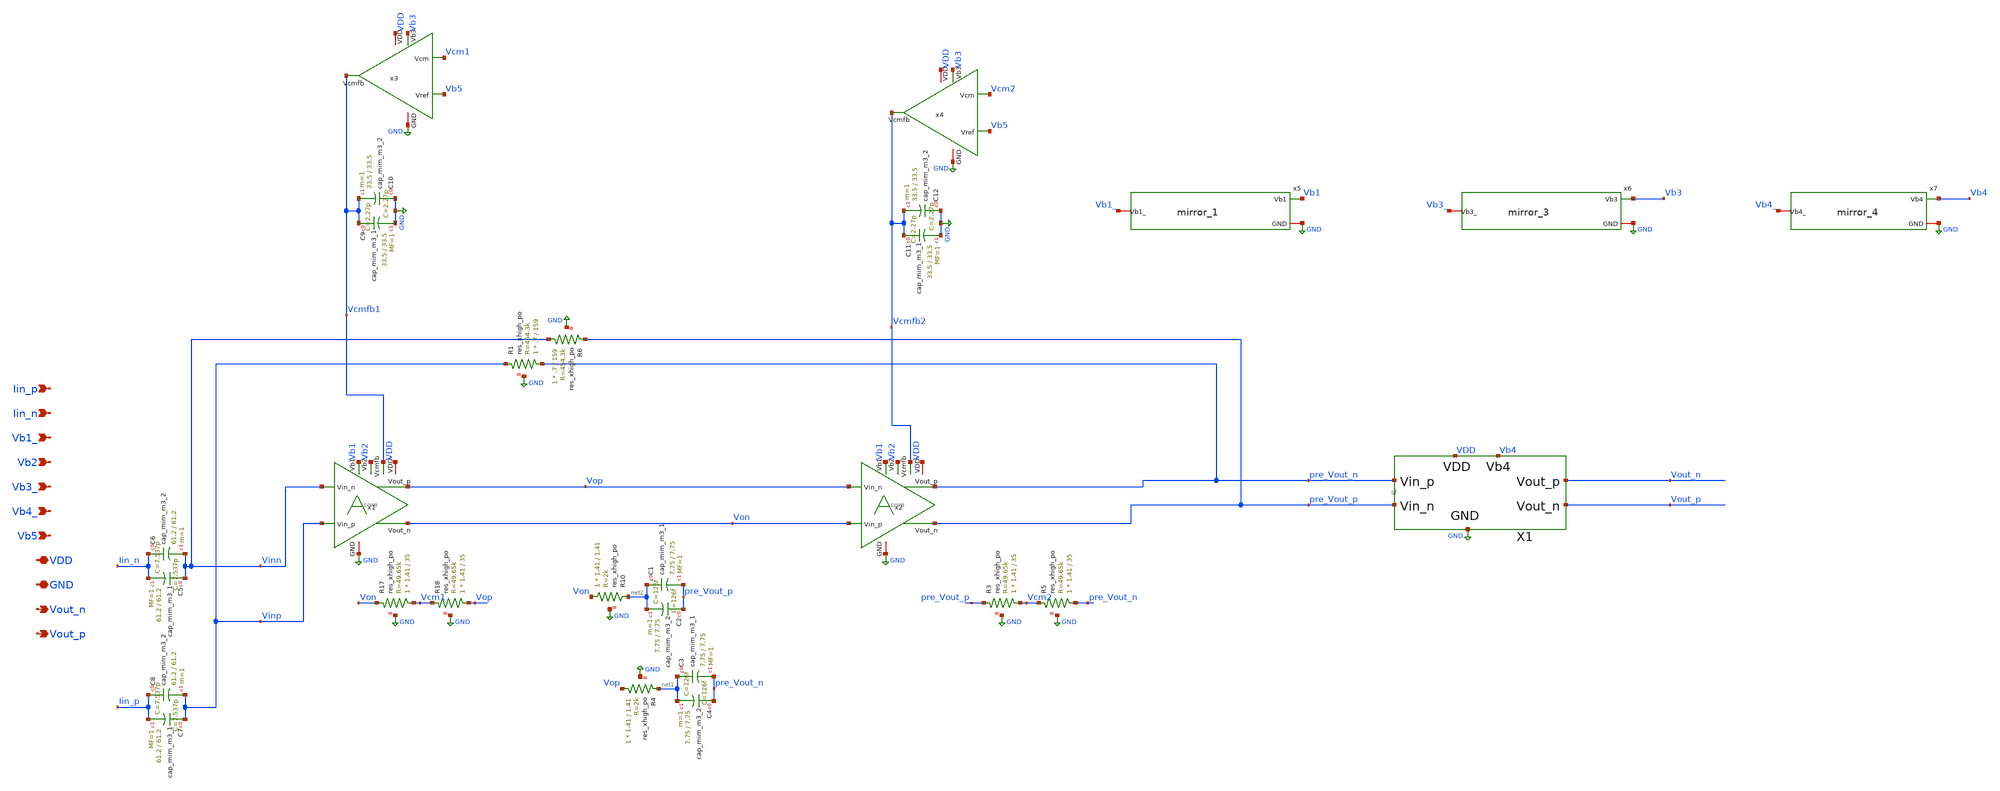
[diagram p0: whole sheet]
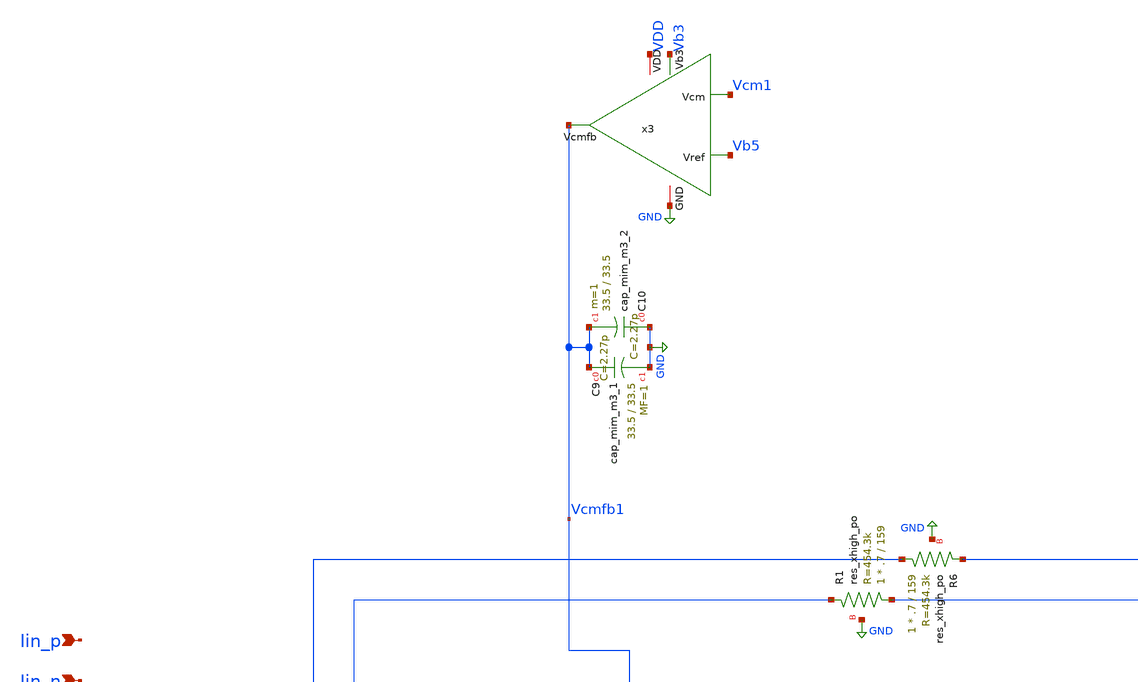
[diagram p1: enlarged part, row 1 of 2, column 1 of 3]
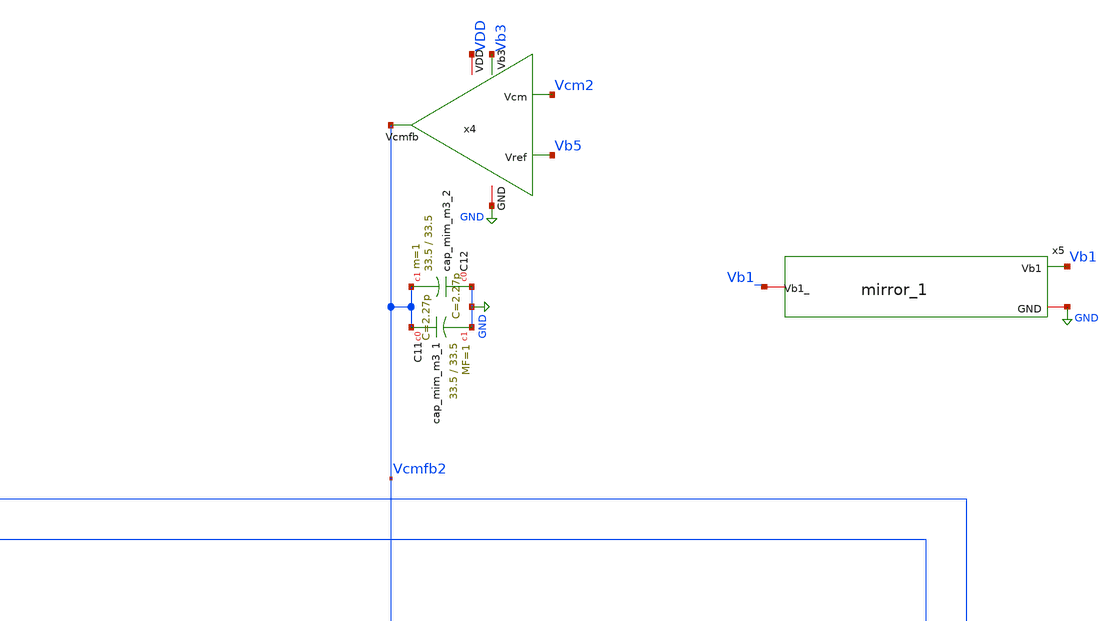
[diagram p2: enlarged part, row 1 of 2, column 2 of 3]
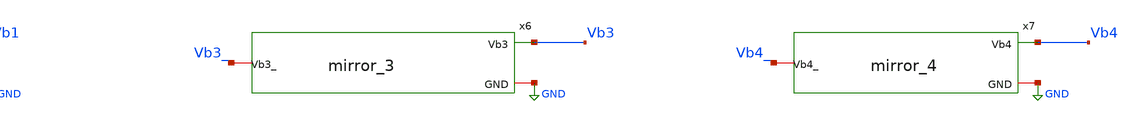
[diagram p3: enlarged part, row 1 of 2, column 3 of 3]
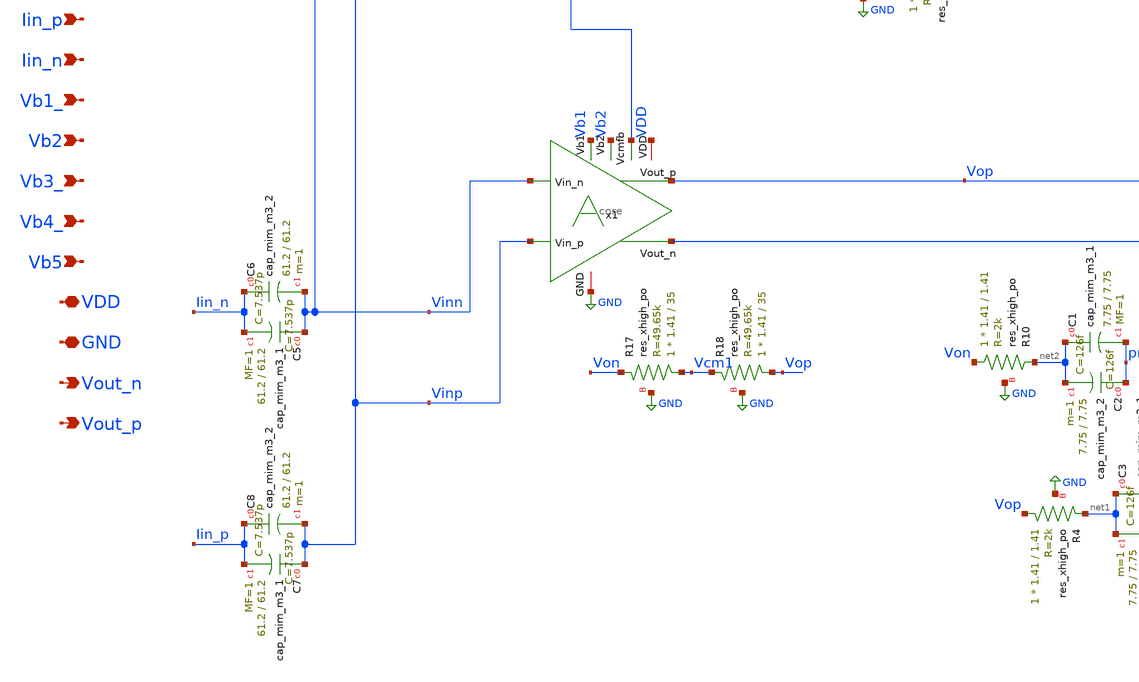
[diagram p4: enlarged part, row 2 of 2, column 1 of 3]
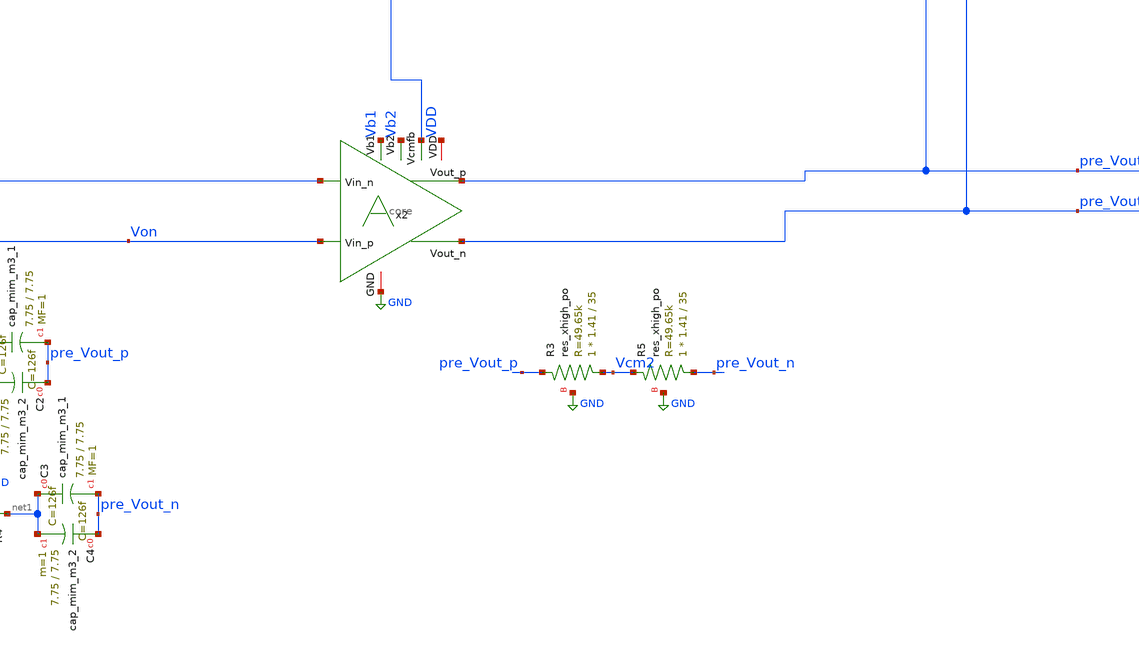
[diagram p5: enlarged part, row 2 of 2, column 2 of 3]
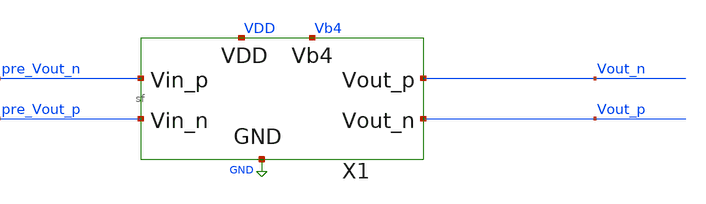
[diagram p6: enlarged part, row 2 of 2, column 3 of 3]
** sch_path: xschem/top.sch
**.subckt top VDD GND Vout_n Iin_n Iin_p Vb1_ Vout_p Vb2 Vb3_ Vb4_ Vb5
*.iopin VDD
*.iopin GND
*.opin Vout_n
*.ipin Iin_n
*.ipin Iin_p
*.ipin Vb1_
*.opin Vout_p
*.ipin Vb2
*.ipin Vb3_
*.ipin Vb4_
*.ipin Vb5
XR6 Vinn pre_Vout_p GND sky130_fd_pr__res_xhigh_po W=.7 L=159 mult=1 m=1
XR1 pre_Vout_n Vinp GND sky130_fd_pr__res_xhigh_po W=.7 L=159 mult=1 m=1
XR3 Vcm2 pre_Vout_p GND sky130_fd_pr__res_xhigh_po W=1.41 L=35 mult=1 m=1
XR5 pre_Vout_n Vcm2 GND sky130_fd_pr__res_xhigh_po W=1.41 L=35 mult=1 m=1
XR4 Vop net1 GND sky130_fd_pr__res_xhigh_po W=1.41 L=1.41 mult=1 m=1
XR10 Von net2 GND sky130_fd_pr__res_xhigh_po W=1.41 L=1.41 mult=1 m=1
XR17 Vcm1 Von GND sky130_fd_pr__res_xhigh_po W=1.41 L=35 mult=1 m=1
XR18 Vop Vcm1 GND sky130_fd_pr__res_xhigh_po W=1.41 L=35 mult=1 m=1
x1 Vinn Vinp Vb2 Vb1 Vcmfb1 VDD GND Vop Von core
x2 Vop Von Vb2 Vb1 Vcmfb2 VDD GND pre_Vout_n pre_Vout_p core
X1 VDD GND pre_Vout_n pre_Vout_p Vout_n Vout_p Vb4 sf
x3 Vcm1 Vb5 Vb3 VDD GND Vcmfb1 cmfb
x4 Vcm2 Vb5 Vb3 VDD GND Vcmfb2 cmfb
x5 Vb1 Vb1_ GND mirror_1
x6 Vb3 Vb3_ GND mirror_3
x7 Vb4 Vb4_ GND mirror_4
XC3 net1 pre_Vout_n sky130_fd_pr__cap_mim_m3_1 W=7.75 L=7.75 MF=1 m=1
XC4 pre_Vout_n net1 sky130_fd_pr__cap_mim_m3_2 W=7.75 L=7.75 MF=1 m=1
XC1 net2 pre_Vout_p sky130_fd_pr__cap_mim_m3_1 W=7.75 L=7.75 MF=1 m=1
XC2 pre_Vout_p net2 sky130_fd_pr__cap_mim_m3_2 W=7.75 L=7.75 MF=1 m=1
XC5 Vinn Iin_n sky130_fd_pr__cap_mim_m3_1 W=61.2 L=61.2 MF=1 m=1
XC6 Iin_n Vinn sky130_fd_pr__cap_mim_m3_2 W=61.2 L=61.2 MF=1 m=1
XC7 Vinp Iin_p sky130_fd_pr__cap_mim_m3_1 W=61.2 L=61.2 MF=1 m=1
XC8 Iin_p Vinp sky130_fd_pr__cap_mim_m3_2 W=61.2 L=61.2 MF=1 m=1
XC9 Vcmfb1 GND sky130_fd_pr__cap_mim_m3_1 W=33.5 L=33.5 MF=1 m=1
XC10 GND Vcmfb1 sky130_fd_pr__cap_mim_m3_2 W=33.5 L=33.5 MF=1 m=1
XC11 Vcmfb2 GND sky130_fd_pr__cap_mim_m3_1 W=33.5 L=33.5 MF=1 m=1
XC12 GND Vcmfb2 sky130_fd_pr__cap_mim_m3_2 W=33.5 L=33.5 MF=1 m=1
**.ends
.GLOBAL GND
.end
